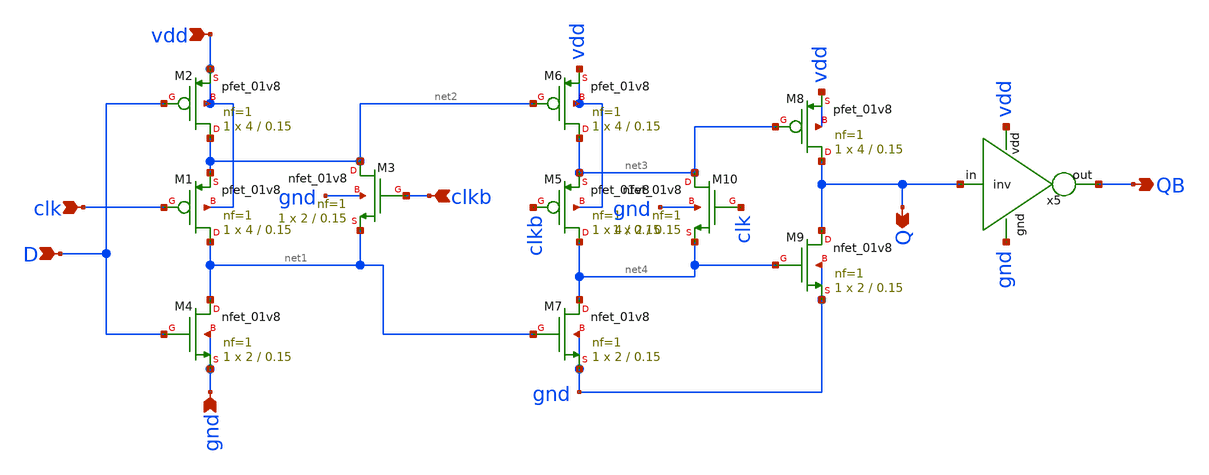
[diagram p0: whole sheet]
** sch_path: pll/dividers_lib/divider_design_trials/Testbench for testing latches/dynamic_cmos_latch.sch
**.subckt dynamic_cmos_latch vdd gnd D QB Q clk clkb
*.ipin vdd
*.ipin gnd
*.ipin D
*.opin QB
*.opin Q
*.ipin clk
*.ipin clkb
XM1 net1 clk net2 vdd sky130_fd_pr__pfet_01v8 L=0.15 W=4 nf=1 ad='int((nf+1)/2) * W/nf * 0.29' as='int((nf+2)/2) * W/nf * 0.29'
+ pd='2*int((nf+1)/2) * (W/nf + 0.29)' ps='2*int((nf+2)/2) * (W/nf + 0.29)' nrd='0.29 / W' nrs='0.29 / W'
+ sa=0 sb=0 sd=0 mult=1 m=1
XM2 net2 D vdd vdd sky130_fd_pr__pfet_01v8 L=0.15 W=4 nf=1 ad='int((nf+1)/2) * W/nf * 0.29' as='int((nf+2)/2) * W/nf * 0.29'
+ pd='2*int((nf+1)/2) * (W/nf + 0.29)' ps='2*int((nf+2)/2) * (W/nf + 0.29)' nrd='0.29 / W' nrs='0.29 / W'
+ sa=0 sb=0 sd=0 mult=1 m=1
XM4 net1 D gnd gnd sky130_fd_pr__nfet_01v8 L=0.15 W=2 nf=1 ad='int((1 + 1)/2) * 2 / 1 * 0.29' as='int((1 + 2)/2) * 2 / 1 * 0.29'
+ pd='2*int((1 + 1)/2) * (2 / 1 + 0.29)' ps='2*int((1 + 2)/2) * (2 / 1 + 0.29)' nrd='0.29 / 2 ' nrs='0.29 / 2 '
+ sa=0 sb=0 sd=0 mult=1 m=1
x5 vdd Q QB gnd inv
XM3 net2 clkb net1 gnd sky130_fd_pr__nfet_01v8 L=0.15 W=2 nf=1 ad='int((1 + 1)/2) * 2 / 1 * 0.29' as='int((1 + 2)/2) * 2 / 1 * 0.29'
+ pd='2*int((1 + 1)/2) * (2 / 1 + 0.29)' ps='2*int((1 + 2)/2) * (2 / 1 + 0.29)' nrd='0.29 / 2 ' nrs='0.29 / 2 '
+ sa=0 sb=0 sd=0 mult=1 m=1
XM5 net4 clkb net3 vdd sky130_fd_pr__pfet_01v8 L=0.15 W=4 nf=1 ad='int((nf+1)/2) * W/nf * 0.29' as='int((nf+2)/2) * W/nf * 0.29'
+ pd='2*int((nf+1)/2) * (W/nf + 0.29)' ps='2*int((nf+2)/2) * (W/nf + 0.29)' nrd='0.29 / W' nrs='0.29 / W'
+ sa=0 sb=0 sd=0 mult=1 m=1
XM6 net3 net2 vdd vdd sky130_fd_pr__pfet_01v8 L=0.15 W=4 nf=1 ad='int((nf+1)/2) * W/nf * 0.29' as='int((nf+2)/2) * W/nf * 0.29'
+ pd='2*int((nf+1)/2) * (W/nf + 0.29)' ps='2*int((nf+2)/2) * (W/nf + 0.29)' nrd='0.29 / W' nrs='0.29 / W'
+ sa=0 sb=0 sd=0 mult=1 m=1
XM7 net4 net1 gnd gnd sky130_fd_pr__nfet_01v8 L=0.15 W=2 nf=1 ad='int((1 + 1)/2) * 2 / 1 * 0.29' as='int((1 + 2)/2) * 2 / 1 * 0.29'
+ pd='2*int((1 + 1)/2) * (2 / 1 + 0.29)' ps='2*int((1 + 2)/2) * (2 / 1 + 0.29)' nrd='0.29 / 2 ' nrs='0.29 / 2 '
+ sa=0 sb=0 sd=0 mult=1 m=1
XM8 Q net3 vdd vdd sky130_fd_pr__pfet_01v8 L=0.15 W=4 nf=1 ad='int((nf+1)/2) * W/nf * 0.29' as='int((nf+2)/2) * W/nf * 0.29'
+ pd='2*int((nf+1)/2) * (W/nf + 0.29)' ps='2*int((nf+2)/2) * (W/nf + 0.29)' nrd='0.29 / W' nrs='0.29 / W'
+ sa=0 sb=0 sd=0 mult=1 m=1
XM9 Q net4 gnd gnd sky130_fd_pr__nfet_01v8 L=0.15 W=2 nf=1 ad='int((1 + 1)/2) * 2 / 1 * 0.29' as='int((1 + 2)/2) * 2 / 1 * 0.29'
+ pd='2*int((1 + 1)/2) * (2 / 1 + 0.29)' ps='2*int((1 + 2)/2) * (2 / 1 + 0.29)' nrd='0.29 / 2 ' nrs='0.29 / 2 '
+ sa=0 sb=0 sd=0 mult=1 m=1
XM10 net3 clk net4 gnd sky130_fd_pr__nfet_01v8 L=0.15 W=2 nf=1 ad='int((1 + 1)/2) * 2 / 1 * 0.29' as='int((1 + 2)/2) * 2 / 1 * 0.29'
+ pd='2*int((1 + 1)/2) * (2 / 1 + 0.29)' ps='2*int((1 + 2)/2) * (2 / 1 + 0.29)' nrd='0.29 / 2 ' nrs='0.29 / 2 '
+ sa=0 sb=0 sd=0 mult=1 m=1
**.ends
.end
